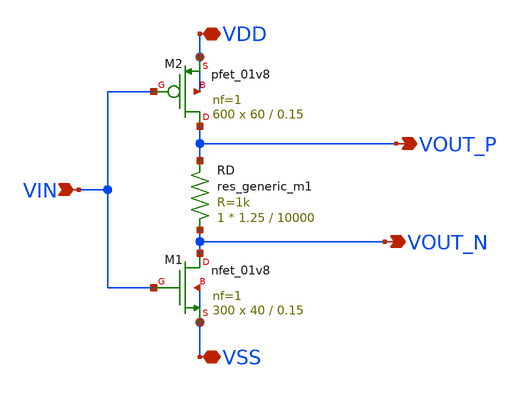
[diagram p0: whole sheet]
** sch_path: xschem/DC_DC_Converter_xschem/OTHERS/DC_DC_Converter_2/DC_DC_Converter/Inverter_4/Inverter4.sch
**.subckt Inverter4 VIN VDD VSS VOUT_P VOUT_N
*.ipin VIN
*.iopin VDD
*.iopin VSS
*.opin VOUT_P
*.opin VOUT_N
XM1 VOUT_N VIN VSS VSS sky130_fd_pr__nfet_01v8 L=0.15 W=40 nf=1 ad='int((nf+1)/2) * W/nf * 0.29' as='int((nf+2)/2) * W/nf * 0.29'
+ pd='2*int((nf+1)/2) * (W/nf + 0.29)' ps='2*int((nf+2)/2) * (W/nf + 0.29)' nrd='0.29 / W' nrs='0.29 / W'
+ sa=0 sb=0 sd=0 mult=300 m=300
XM2 VOUT_P VIN VDD VDD sky130_fd_pr__pfet_01v8 L=0.15 W=60 nf=1 ad='int((nf+1)/2) * W/nf * 0.29' as='int((nf+2)/2) * W/nf * 0.29'
+ pd='2*int((nf+1)/2) * (W/nf + 0.29)' ps='2*int((nf+2)/2) * (W/nf + 0.29)' nrd='0.29 / W' nrs='0.29 / W'
+ sa=0 sb=0 sd=0 mult=600 m=600
RD VOUT_N VOUT_P sky130_fd_pr__res_generic_m1 W=1.25 L=10000 m=1
**.ends
.end
